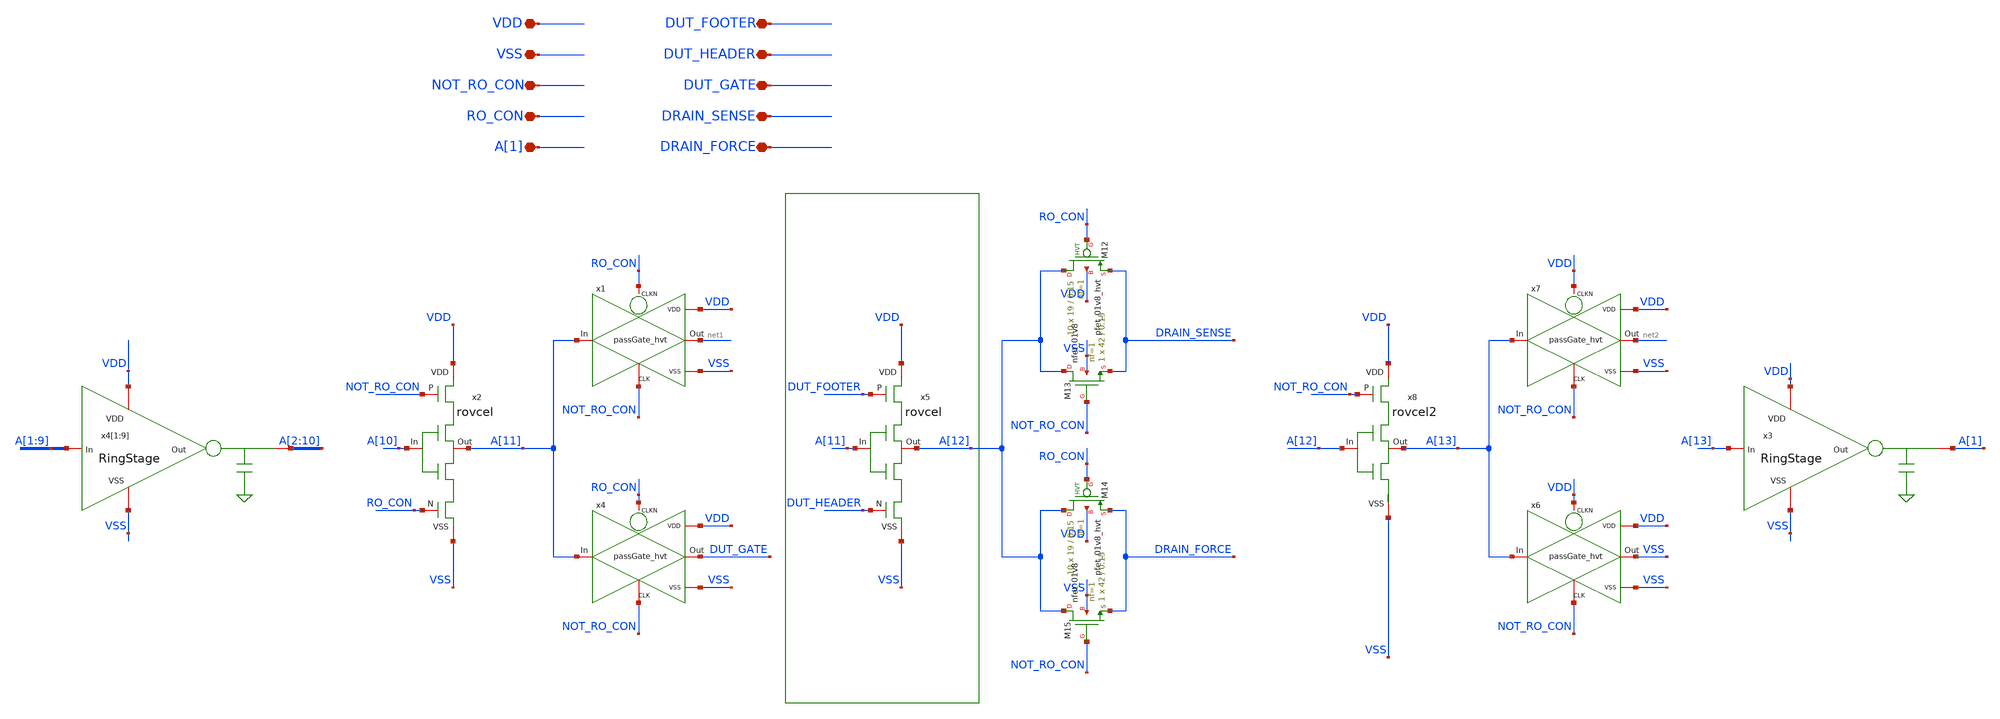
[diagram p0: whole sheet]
** sch_path: HVT/RingOscilator_hvt_13_x10/RingOscilator_hvt_13_x10.sch
**.subckt RingOscilator_hvt_13_x10 VDD VSS NOT_RO_CON RO_CON DUT_FOOTER DUT_HEADER DUT_GATE
*+ DRAIN_SENSE DRAIN_FORCE A[1]
*.iopin VDD
*.iopin VSS
*.iopin NOT_RO_CON
*.iopin RO_CON
*.iopin DUT_FOOTER
*.iopin DUT_HEADER
*.iopin DUT_GATE
*.iopin DRAIN_SENSE
*.iopin DRAIN_FORCE
*.iopin A[1]
x4[1] VDD VSS A[1] A[2] RingStage
x4[2] VDD VSS A[2] A[3] RingStage
x4[3] VDD VSS A[3] A[4] RingStage
x4[4] VDD VSS A[4] A[5] RingStage
x4[5] VDD VSS A[5] A[6] RingStage
x4[6] VDD VSS A[6] A[7] RingStage
x4[7] VDD VSS A[7] A[8] RingStage
x4[8] VDD VSS A[8] A[9] RingStage
x4[9] VDD VSS A[9] A[10] RingStage
x1 A[11] RO_CON VSS VDD NOT_RO_CON net1 passGate_hvt
x4 A[11] RO_CON VSS VDD NOT_RO_CON DUT_GATE passGate_hvt
x6 A[13] VDD VSS VDD NOT_RO_CON VSS passGate_hvt
x7 A[13] VDD VSS VDD NOT_RO_CON net2 passGate_hvt
x3 VDD VSS A[13] A[1] RingStage
XM12 A[12] RO_CON DRAIN_SENSE VDD sky130_fd_pr__pfet_01v8_hvt L=0.15 W=19 nf=1 ad='int((nf+1)/2) * W/nf * 0.29'
+ as='int((nf+2)/2) * W/nf * 0.29' pd='2*int((nf+1)/2) * (W/nf + 0.29)' ps='2*int((nf+2)/2) * (W/nf + 0.29)'
+ nrd='0.29 / W' nrs='0.29 / W' sa=0 sb=0 sd=0 mult=10 m=10
XM13 A[12] NOT_RO_CON DRAIN_SENSE VSS sky130_fd_pr__nfet_01v8 L=0.15 W=42 nf=1 ad='int((nf+1)/2) * W/nf * 0.29'
+ as='int((nf+2)/2) * W/nf * 0.29' pd='2*int((nf+1)/2) * (W/nf + 0.29)' ps='2*int((nf+2)/2) * (W/nf + 0.29)'
+ nrd='0.29 / W' nrs='0.29 / W' sa=0 sb=0 sd=0 mult=1 m=1
XM14 A[12] RO_CON DRAIN_FORCE VDD sky130_fd_pr__pfet_01v8_hvt L=0.15 W=19 nf=1 ad='int((nf+1)/2) * W/nf * 0.29'
+ as='int((nf+2)/2) * W/nf * 0.29' pd='2*int((nf+1)/2) * (W/nf + 0.29)' ps='2*int((nf+2)/2) * (W/nf + 0.29)'
+ nrd='0.29 / W' nrs='0.29 / W' sa=0 sb=0 sd=0 mult=10 m=10
XM15 A[12] NOT_RO_CON DRAIN_FORCE VSS sky130_fd_pr__nfet_01v8 L=0.15 W=42 nf=1 ad='int((nf+1)/2) * W/nf * 0.29'
+ as='int((nf+2)/2) * W/nf * 0.29' pd='2*int((nf+1)/2) * (W/nf + 0.29)' ps='2*int((nf+2)/2) * (W/nf + 0.29)'
+ nrd='0.29 / W' nrs='0.29 / W' sa=0 sb=0 sd=0 mult=1 m=1
x2 VDD VSS A[10] A[11] NOT_RO_CON RO_CON rovcel
x5 VDD VSS A[11] A[12] DUT_FOOTER DUT_HEADER rovcel
x8 VDD VSS A[12] A[13] NOT_RO_CON rovcel2
**.ends
.end
